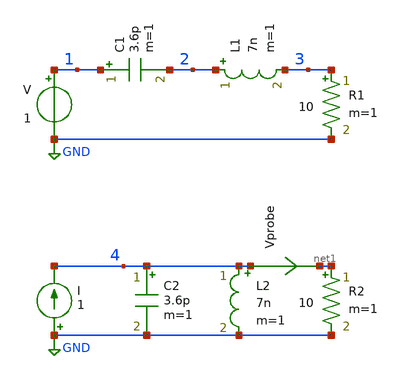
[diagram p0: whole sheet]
** sch_path: rlc_circuit.sch
**.subckt rlc_circuit
V 1 GND 1
C2 4 GND 3.6p m=1
L2 4 GND 7n m=1
R2 net1 GND 10 m=1
C1 1 2 3.6p m=1
L1 2 3 7n m=1
R1 3 GND 10 m=1
I GND 4 1
Vprobe 4 net1 0
.save i(vprobe)
**** begin user architecture code



.option method=gear
.options savecurrents
.save all

.control
  tran 0.01ns 10ns
  alter @V[PULSE] [ 0 1 0 1ns ]
  alter @I[PULSE] [ 0 1m 0 1ns ]

  ***
  alter @V[dc] 0
  alter @V[acmag] 1
  alter r1 = 10
  ac lin 1001 100meg 10000meg

  alter @V[dc] 0
  alter @V[acmag] 1
  alter r1 = 20
  ac lin 1001 100meg 10000meg

  alter @V[dc] 0
  alter @V[acmag] 1
  alter r1 = 40
  ac lin 1001 100meg 10000meg

  ***
  alter @I[dc] 0
  alter @I[acmag] 1
  alter r2 = 160
  ac lin 1001 100meg 10000meg

  alter @I[dc] 0
  alter @I[acmag] 1
  alter r2 = 80
  ac lin 1001 100meg 10000meg

  alter @I[dc] 0
  alter @I[acmag] 1
  alter r2 = 40
  ac lin 1001 100meg 10000meg

  ** impedance plot
  plot xlog ylog db(1/ac3.v#branch) db(ac6.v(4)) db(1/ac2.v#branch) db(ac5.v(4)) db(1/ac1.v#branch)
+ db(ac4.v(4))
  plot xlog ph(1/ac3.v#branch) ph(ac6.v(4)) ph(1/ac2.v#branch) ph(ac5.v(4)) ph(1/ac1.v#branch)
+ ph(ac4.v(4))

.endc

**** end user architecture code
**.ends
.GLOBAL GND
.end
